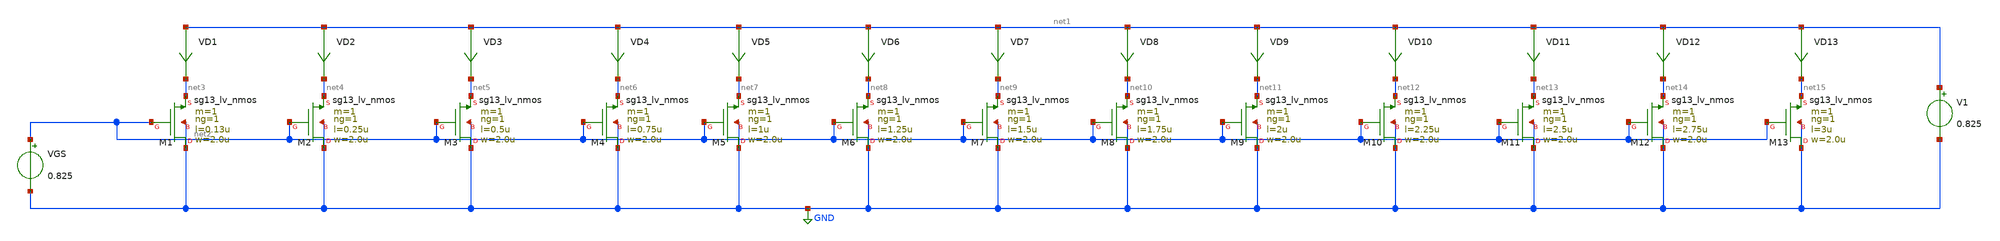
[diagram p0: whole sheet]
** sch_path: Design-Files/gmid_nmos_sg13_lv_nmos_tb.sch
**.subckt gmid_nmos_sg13_lv_nmos_tb
V1 net1 GND 0.825
VGS net2 GND 0.825
VD1 net1 net3 0
.save i(vd1)
VD2 net1 net4 0
.save i(vd2)
VD3 net1 net5 0
.save i(vd3)
VD4 net1 net6 0
.save i(vd4)
VD5 net1 net7 0
.save i(vd5)
VD6 net1 net8 0
.save i(vd6)
VD7 net1 net9 0
.save i(vd7)
VD8 net1 net10 0
.save i(vd8)
VD9 net1 net11 0
.save i(vd9)
VD10 net1 net12 0
.save i(vd10)
VD11 net1 net13 0
.save i(vd11)
VD12 net1 net14 0
.save i(vd12)
VD13 net1 net15 0
.save i(vd13)
XM1 GND net2 net3 GND sg13_lv_nmos w=2.0u l=0.13u ng=1 m=1 mm_ok=1
XM2 GND net2 net4 GND sg13_lv_nmos w=2.0u l=0.25u ng=1 m=1 mm_ok=1
XM3 GND net2 net5 GND sg13_lv_nmos w=2.0u l=0.5u ng=1 m=1 mm_ok=1
XM4 GND net2 net6 GND sg13_lv_nmos w=2.0u l=0.75u ng=1 m=1 mm_ok=1
XM5 GND net2 net7 GND sg13_lv_nmos w=2.0u l=1u ng=1 m=1 mm_ok=1
XM6 GND net2 net8 GND sg13_lv_nmos w=2.0u l=1.25u ng=1 m=1 mm_ok=1
XM7 GND net2 net9 GND sg13_lv_nmos w=2.0u l=1.5u ng=1 m=1 mm_ok=1
XM8 GND net2 net10 GND sg13_lv_nmos w=2.0u l=1.75u ng=1 m=1 mm_ok=1
XM9 GND net2 net11 GND sg13_lv_nmos w=2.0u l=2u ng=1 m=1 mm_ok=1
XM10 GND net2 net12 GND sg13_lv_nmos w=2.0u l=2.25u ng=1 m=1 mm_ok=1
XM11 GND net2 net13 GND sg13_lv_nmos w=2.0u l=2.5u ng=1 m=1 mm_ok=1
XM12 GND net2 net14 GND sg13_lv_nmos w=2.0u l=2.75u ng=1 m=1 mm_ok=1
XM13 GND net2 net15 GND sg13_lv_nmos w=2.0u l=3u ng=1 m=1 mm_ok=1
**** begin user architecture code


.save @n.xm1.nsg13_lv_nmos[gm]
.save @n.xm1.nsg13_lv_nmos[id]
.save @n.xm1.nsg13_lv_nmos[vth]
.save @n.xm1.nsg13_lv_nmos[gds]
.save @n.xm1.nsg13_lv_nmos[cgg]
.save @n.xm1.nsg13_lv_nmos[cgs]
.save @n.xm1.nsg13_lv_nmos[cgd]
.save @n.xm2.nsg13_lv_nmos[gm]
.save @n.xm2.nsg13_lv_nmos[id]
.save @n.xm2.nsg13_lv_nmos[vth]
.save @n.xm2.nsg13_lv_nmos[gds]
.save @n.xm2.nsg13_lv_nmos[cgg]
.save @n.xm2.nsg13_lv_nmos[cgs]
.save @n.xm2.nsg13_lv_nmos[cgd]
.save @n.xm3.nsg13_lv_nmos[gm]
.save @n.xm3.nsg13_lv_nmos[id]
.save @n.xm3.nsg13_lv_nmos[vth]
.save @n.xm3.nsg13_lv_nmos[gds]
.save @n.xm3.nsg13_lv_nmos[cgg]
.save @n.xm3.nsg13_lv_nmos[cgs]
.save @n.xm3.nsg13_lv_nmos[cgd]
.save @n.xm4.nsg13_lv_nmos[gm]
.save @n.xm4.nsg13_lv_nmos[id]
.save @n.xm4.nsg13_lv_nmos[vth]
.save @n.xm4.nsg13_lv_nmos[gds]
.save @n.xm4.nsg13_lv_nmos[cgg]
.save @n.xm4.nsg13_lv_nmos[cgs]
.save @n.xm4.nsg13_lv_nmos[cgd]
.save @n.xm5.nsg13_lv_nmos[gm]
.save @n.xm5.nsg13_lv_nmos[id]
.save @n.xm5.nsg13_lv_nmos[vth]
.save @n.xm5.nsg13_lv_nmos[gds]
.save @n.xm5.nsg13_lv_nmos[cgg]
.save @n.xm5.nsg13_lv_nmos[cgs]
.save @n.xm5.nsg13_lv_nmos[cgd]
.save @n.xm6.nsg13_lv_nmos[gm]
.save @n.xm6.nsg13_lv_nmos[id]
.save @n.xm6.nsg13_lv_nmos[vth]
.save @n.xm6.nsg13_lv_nmos[gds]
.save @n.xm6.nsg13_lv_nmos[cgg]
.save @n.xm6.nsg13_lv_nmos[cgs]
.save @n.xm6.nsg13_lv_nmos[cgd]
.save @n.xm7.nsg13_lv_nmos[gm]
.save @n.xm7.nsg13_lv_nmos[id]
.save @n.xm7.nsg13_lv_nmos[vth]
.save @n.xm7.nsg13_lv_nmos[gds]
.save @n.xm7.nsg13_lv_nmos[cgg]
.save @n.xm7.nsg13_lv_nmos[cgs]
.save @n.xm7.nsg13_lv_nmos[cgd]
.save @n.xm7.nsg13_lv_nmos[gm]
.save @n.xm7.nsg13_lv_nmos[id]
.save @n.xm7.nsg13_lv_nmos[vth]
.save @n.xm7.nsg13_lv_nmos[gds]
.save @n.xm7.nsg13_lv_nmos[cgg]
.save @n.xm7.nsg13_lv_nmos[cgs]
.save @n.xm7.nsg13_lv_nmos[cgd]
.save @n.xm8.nsg13_lv_nmos[gm]
.save @n.xm8.nsg13_lv_nmos[id]
.save @n.xm8.nsg13_lv_nmos[vth]
.save @n.xm8.nsg13_lv_nmos[gds]
.save @n.xm8.nsg13_lv_nmos[cgg]
.save @n.xm8.nsg13_lv_nmos[cgs]
.save @n.xm8.nsg13_lv_nmos[cgd]
.save @n.xm9.nsg13_lv_nmos[gm]
.save @n.xm9.nsg13_lv_nmos[id]
.save @n.xm9.nsg13_lv_nmos[vth]
.save @n.xm9.nsg13_lv_nmos[gds]
.save @n.xm9.nsg13_lv_nmos[cgg]
.save @n.xm9.nsg13_lv_nmos[cgs]
.save @n.xm9.nsg13_lv_nmos[cgd]
.save @n.xm10.nsg13_lv_nmos[gm]
.save @n.xm10.nsg13_lv_nmos[id]
.save @n.xm10.nsg13_lv_nmos[vth]
.save @n.xm10.nsg13_lv_nmos[gds]
.save @n.xm10.nsg13_lv_nmos[cgg]
.save @n.xm10.nsg13_lv_nmos[cgs]
.save @n.xm10.nsg13_lv_nmos[cgd]
.save @n.xm11.nsg13_lv_nmos[gm]
.save @n.xm11.nsg13_lv_nmos[id]
.save @n.xm11.nsg13_lv_nmos[vth]
.save @n.xm11.nsg13_lv_nmos[gds]
.save @n.xm11.nsg13_lv_nmos[cgg]
.save @n.xm11.nsg13_lv_nmos[cgs]
.save @n.xm11.nsg13_lv_nmos[cgd]
.save @n.xm12.nsg13_lv_nmos[gm]
.save @n.xm12.nsg13_lv_nmos[id]
.save @n.xm12.nsg13_lv_nmos[vth]
.save @n.xm12.nsg13_lv_nmos[gds]
.save @n.xm12.nsg13_lv_nmos[cgg]
.save @n.xm12.nsg13_lv_nmos[cgs]
.save @n.xm12.nsg13_lv_nmos[cgd]
.save @n.xm13.nsg13_lv_nmos[gm]
.save @n.xm13.nsg13_lv_nmos[id]
.save @n.xm13.nsg13_lv_nmos[vth]
.save @n.xm13.nsg13_lv_nmos[gds]
.save @n.xm13.nsg13_lv_nmos[cgg]
.save @n.xm13.nsg13_lv_nmos[cgs]
.save @n.xm13.nsg13_lv_nmos[cgd]




.option wnflag=1
.option savecurrents
.temp 27
.control
save all
dc VGS 0.01 1.65 0.1m
remzerovec
write /foss/designs/IHP130_Designs/PDK_CHAR/LV_NMOS/gmid_nmos_sg13_lv_nmos_tb.raw

plot @n.xm1.nsg13_lv_nmos[gm]
plot @n.xm2.nsg13_lv_nmos[gm]
plot @n.xm3.nsg13_lv_nmos[gm]
plot @n.xm4.nsg13_lv_nmos[gm]
plot @n.xm5.nsg13_lv_nmos[gm]
plot @n.xm6.nsg13_lv_nmos[gm]
plot @n.xm7.nsg13_lv_nmos[gm]
plot @n.xm8.nsg13_lv_nmos[gm]
plot @n.xm9.nsg13_lv_nmos[gm]
plot @n.xm10.nsg13_lv_nmos[gm]
plot @n.xm11.nsg13_lv_nmos[gm]
plot @n.xm12.nsg13_lv_nmos[gm]
plot @n.xm13.nsg13_lv_nmos[gm]

wrdata /foss/designs/IHP130_Designs/PDK_CHAR/LV_NMOS/gmid_nmos_1_sg13_lv_nmos_tb.txt
+ @n.xm1.nsg13_lv_nmos[gm] i(VD1) @n.xm1.nsg13_lv_nmos[vth] @n.xm1.nsg13_lv_nmos[gds] @n.xm1.nsg13_lv_nmos[cgg]
+ @n.xm1.nsg13_lv_nmos[cgs] @n.xm1.nsg13_lv_nmos[cgd]
wrdata /foss/designs/IHP130_Designs/PDK_CHAR/LV_NMOS/gmid_nmos_2_sg13_lv_nmos_tb.txt
+ @n.xm2.nsg13_lv_nmos[gm] i(VD2) @n.xm2.nsg13_lv_nmos[vth] @n.xm2.nsg13_lv_nmos[gds] @n.xm2.nsg13_lv_nmos[cgg]
+ @n.xm2.nsg13_lv_nmos[cgs] @n.xm2.nsg13_lv_nmos[cgd]
wrdata /foss/designs/IHP130_Designs/PDK_CHAR/LV_NMOS/gmid_nmos_3_sg13_lv_nmos_tb.txt
+ @n.xm3.nsg13_lv_nmos[gm] i(VD3) @n.xm3.nsg13_lv_nmos[vth] @n.xm3.nsg13_lv_nmos[gds] @n.xm3.nsg13_lv_nmos[cgg]
+ @n.xm3.nsg13_lv_nmos[cgs] @n.xm3.nsg13_lv_nmos[cgd]
wrdata /foss/designs/IHP130_Designs/PDK_CHAR/LV_NMOS/gmid_nmos_4_sg13_lv_nmos_tb.txt
+ @n.xm4.nsg13_lv_nmos[gm] i(VD4) @n.xm4.nsg13_lv_nmos[vth] @n.xm4.nsg13_lv_nmos[gds] @n.xm4.nsg13_lv_nmos[cgg]
+ @n.xm4.nsg13_lv_nmos[cgs] @n.xm4.nsg13_lv_nmos[cgd]
wrdata /foss/designs/IHP130_Designs/PDK_CHAR/LV_NMOS/gmid_nmos_5_sg13_lv_nmos_tb.txt
+ @n.xm5.nsg13_lv_nmos[gm] i(VD5) @n.xm5.nsg13_lv_nmos[vth] @n.xm5.nsg13_lv_nmos[gds] @n.xm5.nsg13_lv_nmos[cgg]
+ @n.xm5.nsg13_lv_nmos[cgs] @n.xm5.nsg13_lv_nmos[cgd]
wrdata /foss/designs/IHP130_Designs/PDK_CHAR/LV_NMOS/gmid_nmos_6_sg13_lv_nmos_tb.txt
+ @n.xm6.nsg13_lv_nmos[gm] i(VD6) @n.xm6.nsg13_lv_nmos[vth] @n.xm6.nsg13_lv_nmos[gds] @n.xm6.nsg13_lv_nmos[cgg]
+ @n.xm6.nsg13_lv_nmos[cgs] @n.xm6.nsg13_lv_nmos[cgd]
wrdata /foss/designs/IHP130_Designs/PDK_CHAR/LV_NMOS/gmid_nmos_7_sg13_lv_nmos_tb.txt
+ @n.xm7.nsg13_lv_nmos[gm] i(VD7) @n.xm7.nsg13_lv_nmos[vth] @n.xm7.nsg13_lv_nmos[gds] @n.xm7.nsg13_lv_nmos[cgg]
+ @n.xm7.nsg13_lv_nmos[cgs] @n.xm7.nsg13_lv_nmos[cgd]
wrdata /foss/designs/IHP130_Designs/PDK_CHAR/LV_NMOS/gmid_nmos_8_sg13_lv_nmos_tb.txt
+ @n.xm8.nsg13_lv_nmos[gm] i(VD8) @n.xm8.nsg13_lv_nmos[vth] @n.xm8.nsg13_lv_nmos[gds] @n.xm8.nsg13_lv_nmos[cgg]
+ @n.xm8.nsg13_lv_nmos[cgs] @n.xm8.nsg13_lv_nmos[cgd]
wrdata /foss/designs/IHP130_Designs/PDK_CHAR/LV_NMOS/gmid_nmos_9_sg13_lv_nmos_tb.txt
+ @n.xm9.nsg13_lv_nmos[gm] i(VD9) @n.xm9.nsg13_lv_nmos[vth] @n.xm9.nsg13_lv_nmos[gds] @n.xm9.nsg13_lv_nmos[cgg]
+ @n.xm9.nsg13_lv_nmos[cgs] @n.xm9.nsg13_lv_nmos[cgd]
wrdata /foss/designs/IHP130_Designs/PDK_CHAR/LV_NMOS/gmid_nmos_10_sg13_lv_nmos_tb.txt
+ @n.xm10.nsg13_lv_nmos[gm] i(VD10) @n.xm10.nsg13_lv_nmos[vth] @n.xm10.nsg13_lv_nmos[gds] @n.xm10.nsg13_lv_nmos[cgg]
+ @n.xm10.nsg13_lv_nmos[cgs] @n.xm10.nsg13_lv_nmos[cgd]
wrdata /foss/designs/IHP130_Designs/PDK_CHAR/LV_NMOS/gmid_nmos_11_sg13_lv_nmos_tb.txt
+ @n.xm11.nsg13_lv_nmos[gm] i(VD11) @n.xm11.nsg13_lv_nmos[vth] @n.xm11.nsg13_lv_nmos[gds] @n.xm11.nsg13_lv_nmos[cgg]
+ @n.xm11.nsg13_lv_nmos[cgs] @n.xm11.nsg13_lv_nmos[cgd]
wrdata /foss/designs/IHP130_Designs/PDK_CHAR/LV_NMOS/gmid_nmos_12_sg13_lv_nmos_tb.txt
+ @n.xm12.nsg13_lv_nmos[gm] i(VD12) @n.xm12.nsg13_lv_nmos[vth] @n.xm12.nsg13_lv_nmos[gds] @n.xm12.nsg13_lv_nmos[cgg]
+ @n.xm12.nsg13_lv_nmos[cgs] @n.xm12.nsg13_lv_nmos[cgd]
wrdata /foss/designs/IHP130_Designs/PDK_CHAR/LV_NMOS/gmid_nmos_13_sg13_lv_nmos_tb.txt
+ @n.xm13.nsg13_lv_nmos[gm] i(VD13) @n.xm13.nsg13_lv_nmos[vth] @n.xm13.nsg13_lv_nmos[gds] @n.xm13.nsg13_lv_nmos[cgg]
+ @n.xm13.nsg13_lv_nmos[cgs] @n.xm13.nsg13_lv_nmos[cgd]

set appendwrite
op
remzerovec
write /foss/designs/IHP130_Designs/PDK_CHAR/LV_NMOS/gmid_nmos_sg13_lv_nmos_tb.raw
quit 0
.endc



.lib cornerMOSlv.lib mos_tt

**** end user architecture code
**.ends
.GLOBAL GND
.end
